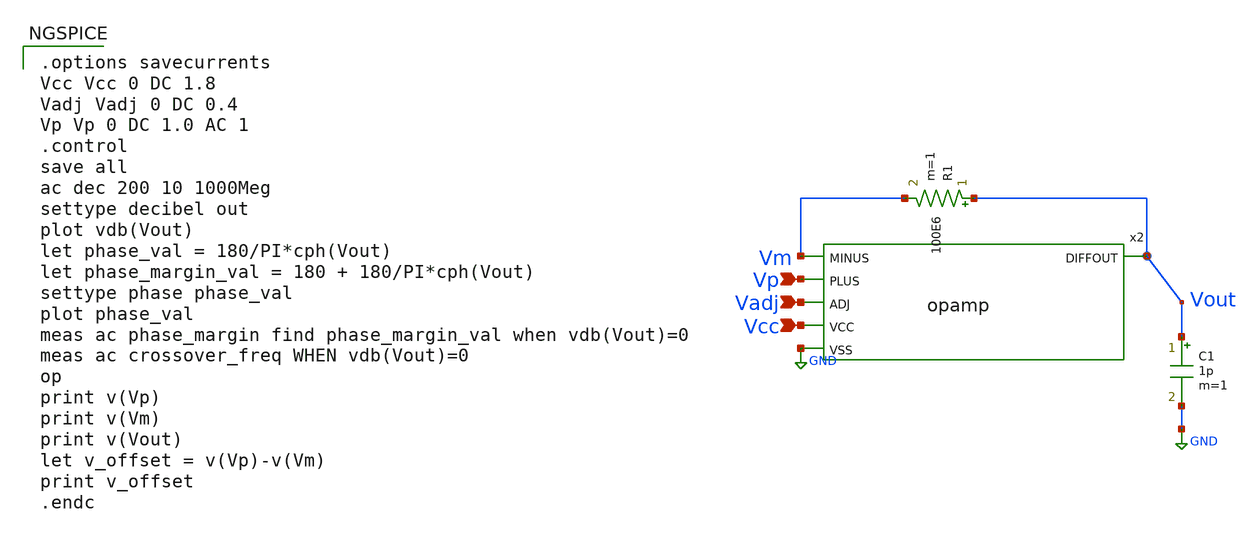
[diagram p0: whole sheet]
** sch_path: schematic/test_ac.sch
**.subckt test_ac Vp Vcc Vadj
*.ipin Vp
*.ipin Vcc
*.ipin Vadj
R1 Vout Vm 100E6 m=1
x2 Vout Vm Vp Vadj Vcc GND opamp
C1 Vout GND 1p m=1
**** begin user architecture code

.options savecurrents
Vcc Vcc 0 DC 1.8
Vadj Vadj 0 DC 0.4
Vp Vp 0 DC 1.0 AC 1
.control
save all
ac dec 200 10 1000Meg
settype decibel out
plot vdb(Vout)
let phase_val = 180/PI*cph(Vout)
let phase_margin_val = 180 + 180/PI*cph(Vout)
settype phase phase_val
plot phase_val
meas ac phase_margin find phase_margin_val when vdb(Vout)=0
meas ac crossover_freq WHEN vdb(Vout)=0
op
print v(Vp)
print v(Vm)
print v(Vout)
let v_offset = v(Vp)-v(Vm)
print v_offset
.endc



** opencircuitdesign pdks install
.lib $::SKYWATER_MODELS/sky130.lib.spice tt


**** end user architecture code
**.ends

* expanding   symbol:  opamp.sym # of pins=6
** sym_path: schematic/opamp.sym
** sch_path: schematic/opamp.sch
.subckt opamp DIFFOUT MINUS PLUS ADJ VCC VSS
*.ipin PLUS
*.ipin MINUS
*.ipin VSS
*.ipin VCC
*.opin DIFFOUT
*.ipin ADJ
C6 G1 0 2f m=1
XM18 G2 G2 net6 VSS sky130_fd_pr__nfet_01v8_lvt L=4 W=2 nf=1 ad='W * 0.29' as='W * 0.29' pd='2*(W + 0.29)'
+ ps='2*(W + 0.29)' nrd=0 nrs=0 sa=0 sb=0 sd=0 mult=1 m=1
XM2 G1 G1 net7 VSS sky130_fd_pr__nfet_01v8_lvt L=4 W=2 nf=1 ad='W * 0.29' as='W * 0.29' pd='2*(W + 0.29)'
+ ps='2*(W + 0.29)' nrd=0 nrs=0 sa=0 sb=0 sd=0 mult=1 m=1
XMR G2 PLUS net8 VCC sky130_fd_pr__pfet_01v8_lvt L=2 W=8 nf=1 ad='W * 0.29' as='W * 0.29' pd='2*(W + 0.29)'
+ ps='2*(W + 0.29)' nrd=0 nrs=0 sa=0 sb=0 sd=0 mult=1 m=1
XML G1 MINUS net9 VCC sky130_fd_pr__pfet_01v8_lvt L=2 W=8 nf=1 ad='W * 0.29' as='W * 0.29' pd='2*(W + 0.29)'
+ ps='2*(W + 0.29)' nrd=0 nrs=0 sa=0 sb=0 sd=0 mult=1 m=1
v1 SP net9 0
.save i(v1)
C4 SP 0 2f m=1
C1 G2 0 2f m=1
C5 DIFFOUT 0 4f m=1
XM6 DIFFOUT G2 net1 VSS sky130_fd_pr__nfet_01v8_lvt L=4 W=2 nf=1 ad='W * 0.29' as='W * 0.29' pd='2*(W + 0.29)'
+ ps='2*(W + 0.29)' nrd=0 nrs=0 sa=0 sb=0 sd=0 mult=1 m=1
v2 SP net8 0
.save i(v2)
v4 net1 VSS 0
.save i(v4)
v6 VCC SP 0
.save i(v6)
v17 VCC net3 0
.save i(v17)
XM12 net2 G1 VSS VSS sky130_fd_pr__nfet_01v8_lvt L=4 W=2 nf=1 ad='W * 0.29' as='W * 0.29' pd='2*(W + 0.29)'
+ ps='2*(W + 0.29)' nrd=0 nrs=0 sa=0 sb=0 sd=0 mult=1 m=1
XM54 net2 net2 net3 VCC sky130_fd_pr__pfet_01v8_lvt L=4 W=4 nf=1 ad='W * 0.29' as='W * 0.29' pd='2*(W + 0.29)'
+ ps='2*(W + 0.29)' nrd=0 nrs=0 sa=0 sb=0 sd=0 mult=1 m=1
XM5 DIFFOUT net2 net3 VCC sky130_fd_pr__pfet_01v8_lvt L=4 W=4 nf=1 ad='W * 0.29' as='W * 0.29' pd='2*(W + 0.29)'
+ ps='2*(W + 0.29)' nrd=0 nrs=0 sa=0 sb=0 sd=0 mult=1 m=1
XM8 net4 ADJ VCC VCC sky130_fd_pr__pfet_01v8_lvt L=1 W=1 nf=1 ad='W * 0.29' as='W * 0.29' pd='W + 2 * 0.29'
+ ps='W + 2 * 0.29' nrd=0 nrs=0 sa=0 sb=0 sd=0 mult=1 m=1
XM9 net4 ADJ net5 VSS sky130_fd_pr__nfet_01v8_lvt L=1 W=0.5 nf=1 ad='W * 0.29' as='W * 0.29' pd='W + 2 * 0.29'
+ ps='W + 2 * 0.29' nrd=0 nrs=0 sa=0 sb=0 sd=0 mult=1 m=1
XM10 net5 VCC VSS VSS sky130_fd_pr__nfet_01v8_lvt L=8 W=0.5 nf=1 ad='W * 0.29' as='W * 0.29' pd='2*(W + 0.29)'
+ ps='2*(W + 0.29)' nrd=0 nrs=0 sa=0 sb=0 sd=0 mult=1 m=1
v3 net4 G1 0
.save i(v3)
v5 net6 VSS 0
.save i(v5)
v7 net7 VSS 0
.save i(v7)
.ends

.GLOBAL GND
.end
